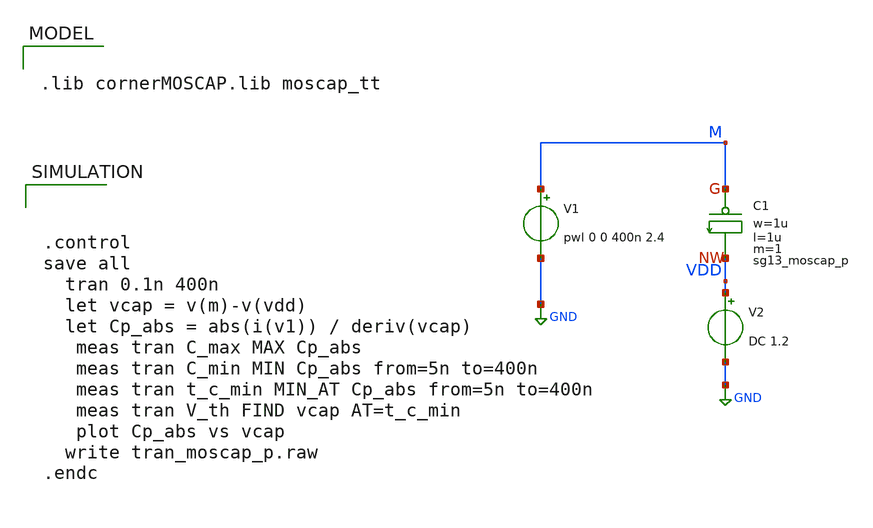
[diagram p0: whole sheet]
** sch_path: ihp-sg13g2/libs.tech/xschem/sg13g2_tests/tran_moscap_p.sch
**.subckt tran_moscap_p
V1 M GND pwl 0 0 400n 2.4
XC1 M VDD sg13_moscap_p w=1u l=1u m=1 mm_ok=1
V2 VDD GND DC 1.2
**** begin user architecture code


.lib cornerMOSCAP.lib moscap_tt





.control
save all
  tran 0.1n 400n
  let vcap = v(m)-v(vdd)
  let Cp_abs = abs(i(v1)) / deriv(vcap)
   meas tran C_max MAX Cp_abs
   meas tran C_min MIN Cp_abs from=5n to=400n
   meas tran t_c_min MIN_AT Cp_abs from=5n to=400n
   meas tran V_th FIND vcap AT=t_c_min
   plot Cp_abs vs vcap
  write tran_moscap_p.raw
.endc



**** end user architecture code
**.ends
.GLOBAL GND
.end
